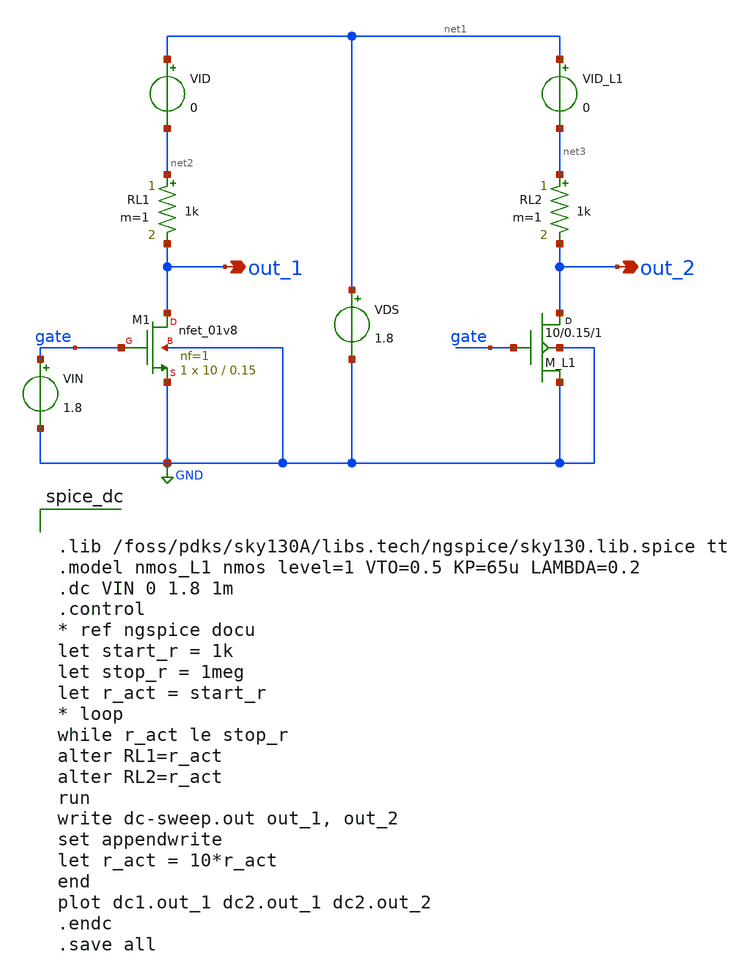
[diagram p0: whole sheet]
** sch_path: designs/nmost_r_inv.sch
**.subckt nmost_r_inv out_1 out_2
*.opin out_1
*.opin out_2
XM1 out_1 gate GND GND sky130_fd_pr__nfet_01v8 L=0.15 W=10 nf=1 ad='int((nf+1)/2) * W/nf * 0.29' as='int((nf+2)/2) * W/nf * 0.29'
+ pd='2*int((nf+1)/2) * (W/nf + 0.29)' ps='2*int((nf+2)/2) * (W/nf + 0.29)' nrd='0.29 / W' nrs='0.29 / W'
+ sa=0 sb=0 sd=0 mult=1 m=1
VIN gate GND 1.8
VDS net1 GND 1.8
VID net1 net2 0
M_L1 out_2 gate GND GND nmos_L1 w=10 l=0.15 m=1
VID_L1 net1 net3 0
RL1 net2 out_1 1k m=1
RL2 net3 out_2 1k m=1
**** begin user architecture code


.lib /foss/pdks/sky130A/libs.tech/ngspice/sky130.lib.spice tt
.model nmos_L1 nmos level=1 VTO=0.5 KP=65u LAMBDA=0.2
.dc VIN 0 1.8 1m
.control
* ref ngspice docu
let start_r = 1k
let stop_r = 1meg
let r_act = start_r
* loop
while r_act le stop_r
alter RL1=r_act
alter RL2=r_act
run
write dc-sweep.out out_1, out_2
set appendwrite
let r_act = 10*r_act
end
plot dc1.out_1 dc2.out_1 dc2.out_2
.endc
.save all

**** end user architecture code
**.ends
.GLOBAL GND
.end
